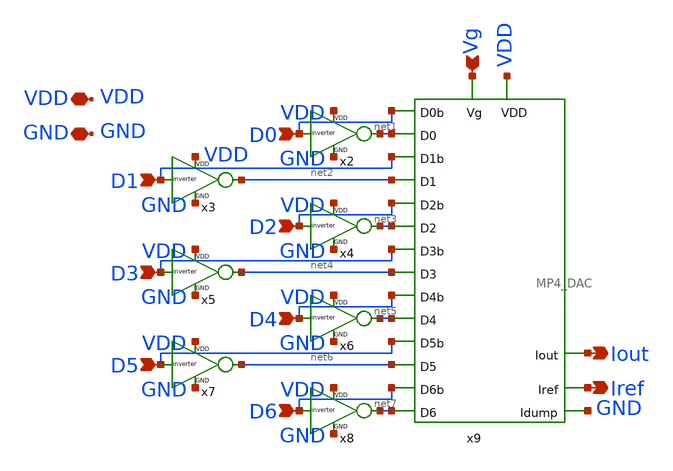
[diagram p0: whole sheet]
** sch_path: Final DAC files/schematics/DAC/simple_MP4_DAC.sch
**.subckt simple_MP4_DAC Iout D0 D1 D2 D3 D4 D5 D6 VDD GND Iref Vg
*.opin Iout
*.ipin D0
*.ipin D1
*.ipin D2
*.ipin D3
*.ipin D4
*.ipin D5
*.ipin D6
*.iopin VDD
*.iopin GND
*.opin Iref
*.ipin Vg
x2 VDD D0 net1 GND inverter
x3 VDD D1 net2 GND inverter
x4 VDD D2 net3 GND inverter
x5 VDD D3 net4 GND inverter
x6 VDD D4 net5 GND inverter
x7 VDD D5 net6 GND inverter
x8 VDD D6 net7 GND inverter
x9 VDD Vg net1 net3 net4 net5 net6 D5 net2 D0 D1 D2 D3 D4 net7 D6 Iref GND Iout MP4_DAC
**.ends

* expanding   symbol:  /home/madvlsi/dev/git/7-bit-D-A-converter-MP4-MADVLSI/schematics/ieee
*+ DAC/inverter.sym # of pins=4
** sym_path: schematics/ieee DAC/inverter.sym
** sch_path: schematics/ieee DAC/inverter.sch
.subckt inverter VDD A Y GND
*.ipin A
*.iopin VDD
*.iopin GND
*.opin Y
XM1 Y A GND GND sky130_fd_pr__nfet_01v8 L=0.5 W=12 nf=1 ad='int((nf+1)/2) * W/nf * 0.29' as='int((nf+2)/2) * W/nf * 0.29'
+ pd='2*int((nf+1)/2) * (W/nf + 0.29)' ps='2*int((nf+2)/2) * (W/nf + 0.29)' nrd='0.29 / W' nrs='0.29 / W'
+ sa=0 sb=0 sd=0 mult=1 m=1
XM2 Y A VDD VDD sky130_fd_pr__pfet_01v8 L=0.5 W=12 nf=1 ad='int((nf+1)/2) * W/nf * 0.29' as='int((nf+2)/2) * W/nf * 0.29'
+ pd='2*int((nf+1)/2) * (W/nf + 0.29)' ps='2*int((nf+2)/2) * (W/nf + 0.29)' nrd='0.29 / W' nrs='0.29 / W'
+ sa=0 sb=0 sd=0 mult=1 m=1
.ends


* expanding   symbol:  /home/madvlsi/dev/git/7-bit-D-A-converter-MP4-MADVLSI/Final DAC
*+ files/schematics/DAC/MP4_DAC.sym # of pins=19
** sym_path: Final DAC files/schematics/DAC/MP4_DAC.sym
** sch_path: Final DAC files/schematics/DAC/MP4_DAC.sch
.subckt MP4_DAC VDD Vg D0 D2 D3 D4 D5 D5b D1 D0b D1b D2b D3b D4b D6 D6b Iref Idump Iout
*.ipin Iout
*.ipin Vg
*.opin Iref
*.opin Idump
*.iopin VDD
*.ipin D0
*.ipin D1
*.ipin D2
*.ipin D3
*.ipin D4
*.ipin D5
*.ipin D6
*.ipin D0b
*.ipin D1b
*.ipin D2b
*.ipin D3b
*.ipin D4b
*.ipin D5b
*.ipin D6b
XM5 net7 Vg Iout GND sky130_fd_pr__nfet_01v8 L=4 W=16 nf=1 ad='int((nf+1)/2) * W/nf * 0.29' as='int((nf+2)/2) * W/nf * 0.29'
+ pd='2*int((nf+1)/2) * (W/nf + 0.29)' ps='2*int((nf+2)/2) * (W/nf + 0.29)' nrd='0.29 / W' nrs='0.29 / W'
+ sa=0 sb=0 sd=0 mult=2 m=2
XM8 net7 Vg net1 GND sky130_fd_pr__nfet_01v8 L=4 W=16 nf=1 ad='int((nf+1)/2) * W/nf * 0.29' as='int((nf+2)/2) * W/nf * 0.29'
+ pd='2*int((nf+1)/2) * (W/nf + 0.29)' ps='2*int((nf+2)/2) * (W/nf + 0.29)' nrd='0.29 / W' nrs='0.29 / W'
+ sa=0 sb=0 sd=0 mult=2 m=2
XM9 net1 Vg VDD GND sky130_fd_pr__nfet_01v8 L=4 W=16 nf=1 ad='int((nf+1)/2) * W/nf * 0.29' as='int((nf+2)/2) * W/nf * 0.29'
+ pd='2*int((nf+1)/2) * (W/nf + 0.29)' ps='2*int((nf+2)/2) * (W/nf + 0.29)' nrd='0.29 / W' nrs='0.29 / W'
+ sa=0 sb=0 sd=0 mult=1 m=1
XM12 net1 Vg net2 GND sky130_fd_pr__nfet_01v8 L=4 W=16 nf=1 ad='int((nf+1)/2) * W/nf * 0.29' as='int((nf+2)/2) * W/nf * 0.29'
+ pd='2*int((nf+1)/2) * (W/nf + 0.29)' ps='2*int((nf+2)/2) * (W/nf + 0.29)' nrd='0.29 / W' nrs='0.29 / W'
+ sa=0 sb=0 sd=0 mult=2 m=2
XM13 net2 Vg VDD GND sky130_fd_pr__nfet_01v8 L=4 W=16 nf=1 ad='int((nf+1)/2) * W/nf * 0.29' as='int((nf+2)/2) * W/nf * 0.29'
+ pd='2*int((nf+1)/2) * (W/nf + 0.29)' ps='2*int((nf+2)/2) * (W/nf + 0.29)' nrd='0.29 / W' nrs='0.29 / W'
+ sa=0 sb=0 sd=0 mult=1 m=1
XM16 net2 Vg net3 GND sky130_fd_pr__nfet_01v8 L=4 W=16 nf=1 ad='int((nf+1)/2) * W/nf * 0.29' as='int((nf+2)/2) * W/nf * 0.29'
+ pd='2*int((nf+1)/2) * (W/nf + 0.29)' ps='2*int((nf+2)/2) * (W/nf + 0.29)' nrd='0.29 / W' nrs='0.29 / W'
+ sa=0 sb=0 sd=0 mult=2 m=2
XM17 net3 Vg VDD GND sky130_fd_pr__nfet_01v8 L=4 W=16 nf=1 ad='int((nf+1)/2) * W/nf * 0.29' as='int((nf+2)/2) * W/nf * 0.29'
+ pd='2*int((nf+1)/2) * (W/nf + 0.29)' ps='2*int((nf+2)/2) * (W/nf + 0.29)' nrd='0.29 / W' nrs='0.29 / W'
+ sa=0 sb=0 sd=0 mult=1 m=1
XM7 net3 Vg net4 GND sky130_fd_pr__nfet_01v8 L=4 W=16 nf=1 ad='int((nf+1)/2) * W/nf * 0.29' as='int((nf+2)/2) * W/nf * 0.29'
+ pd='2*int((nf+1)/2) * (W/nf + 0.29)' ps='2*int((nf+2)/2) * (W/nf + 0.29)' nrd='0.29 / W' nrs='0.29 / W'
+ sa=0 sb=0 sd=0 mult=2 m=2
XM10 net4 Vg VDD GND sky130_fd_pr__nfet_01v8 L=4 W=16 nf=1 ad='int((nf+1)/2) * W/nf * 0.29' as='int((nf+2)/2) * W/nf * 0.29'
+ pd='2*int((nf+1)/2) * (W/nf + 0.29)' ps='2*int((nf+2)/2) * (W/nf + 0.29)' nrd='0.29 / W' nrs='0.29 / W'
+ sa=0 sb=0 sd=0 mult=1 m=1
XM15 net4 Vg net5 GND sky130_fd_pr__nfet_01v8 L=4 W=16 nf=1 ad='int((nf+1)/2) * W/nf * 0.29' as='int((nf+2)/2) * W/nf * 0.29'
+ pd='2*int((nf+1)/2) * (W/nf + 0.29)' ps='2*int((nf+2)/2) * (W/nf + 0.29)' nrd='0.29 / W' nrs='0.29 / W'
+ sa=0 sb=0 sd=0 mult=2 m=2
XM18 net5 Vg VDD GND sky130_fd_pr__nfet_01v8 L=4 W=16 nf=1 ad='int((nf+1)/2) * W/nf * 0.29' as='int((nf+2)/2) * W/nf * 0.29'
+ pd='2*int((nf+1)/2) * (W/nf + 0.29)' ps='2*int((nf+2)/2) * (W/nf + 0.29)' nrd='0.29 / W' nrs='0.29 / W'
+ sa=0 sb=0 sd=0 mult=1 m=1
XM28 net5 Vg net6 GND sky130_fd_pr__nfet_01v8 L=4 W=16 nf=1 ad='int((nf+1)/2) * W/nf * 0.29' as='int((nf+2)/2) * W/nf * 0.29'
+ pd='2*int((nf+1)/2) * (W/nf + 0.29)' ps='2*int((nf+2)/2) * (W/nf + 0.29)' nrd='0.29 / W' nrs='0.29 / W'
+ sa=0 sb=0 sd=0 mult=2 m=2
XM29 net6 Vg VDD GND sky130_fd_pr__nfet_01v8 L=4 W=16 nf=1 ad='int((nf+1)/2) * W/nf * 0.29' as='int((nf+2)/2) * W/nf * 0.29'
+ pd='2*int((nf+1)/2) * (W/nf + 0.29)' ps='2*int((nf+2)/2) * (W/nf + 0.29)' nrd='0.29 / W' nrs='0.29 / W'
+ sa=0 sb=0 sd=0 mult=2 m=2
XM1 net1 D5 Iref GND sky130_fd_pr__nfet_01v8 L=4 W=16 nf=1 ad='int((nf+1)/2) * W/nf * 0.29' as='int((nf+2)/2) * W/nf * 0.29'
+ pd='2*int((nf+1)/2) * (W/nf + 0.29)' ps='2*int((nf+2)/2) * (W/nf + 0.29)' nrd='0.29 / W' nrs='0.29 / W'
+ sa=0 sb=0 sd=0 mult=1 m=1
XM4 Idump D5b net1 GND sky130_fd_pr__nfet_01v8 L=4 W=16 nf=1 ad='int((nf+1)/2) * W/nf * 0.29' as='int((nf+2)/2) * W/nf * 0.29'
+ pd='2*int((nf+1)/2) * (W/nf + 0.29)' ps='2*int((nf+2)/2) * (W/nf + 0.29)' nrd='0.29 / W' nrs='0.29 / W'
+ sa=0 sb=0 sd=0 mult=1 m=1
XM30 net2 D4 Iref GND sky130_fd_pr__nfet_01v8 L=4 W=16 nf=1 ad='int((nf+1)/2) * W/nf * 0.29' as='int((nf+2)/2) * W/nf * 0.29'
+ pd='2*int((nf+1)/2) * (W/nf + 0.29)' ps='2*int((nf+2)/2) * (W/nf + 0.29)' nrd='0.29 / W' nrs='0.29 / W'
+ sa=0 sb=0 sd=0 mult=1 m=1
XM31 Idump D4b net2 GND sky130_fd_pr__nfet_01v8 L=4 W=16 nf=1 ad='int((nf+1)/2) * W/nf * 0.29' as='int((nf+2)/2) * W/nf * 0.29'
+ pd='2*int((nf+1)/2) * (W/nf + 0.29)' ps='2*int((nf+2)/2) * (W/nf + 0.29)' nrd='0.29 / W' nrs='0.29 / W'
+ sa=0 sb=0 sd=0 mult=1 m=1
XM32 net3 D3 Iref GND sky130_fd_pr__nfet_01v8 L=4 W=16 nf=1 ad='int((nf+1)/2) * W/nf * 0.29' as='int((nf+2)/2) * W/nf * 0.29'
+ pd='2*int((nf+1)/2) * (W/nf + 0.29)' ps='2*int((nf+2)/2) * (W/nf + 0.29)' nrd='0.29 / W' nrs='0.29 / W'
+ sa=0 sb=0 sd=0 mult=1 m=1
XM33 Idump D3b net3 GND sky130_fd_pr__nfet_01v8 L=4 W=16 nf=1 ad='int((nf+1)/2) * W/nf * 0.29' as='int((nf+2)/2) * W/nf * 0.29'
+ pd='2*int((nf+1)/2) * (W/nf + 0.29)' ps='2*int((nf+2)/2) * (W/nf + 0.29)' nrd='0.29 / W' nrs='0.29 / W'
+ sa=0 sb=0 sd=0 mult=1 m=1
XM34 net4 D2 Iref GND sky130_fd_pr__nfet_01v8 L=4 W=16 nf=1 ad='int((nf+1)/2) * W/nf * 0.29' as='int((nf+2)/2) * W/nf * 0.29'
+ pd='2*int((nf+1)/2) * (W/nf + 0.29)' ps='2*int((nf+2)/2) * (W/nf + 0.29)' nrd='0.29 / W' nrs='0.29 / W'
+ sa=0 sb=0 sd=0 mult=1 m=1
XM35 Idump D2b net4 GND sky130_fd_pr__nfet_01v8 L=4 W=16 nf=1 ad='int((nf+1)/2) * W/nf * 0.29' as='int((nf+2)/2) * W/nf * 0.29'
+ pd='2*int((nf+1)/2) * (W/nf + 0.29)' ps='2*int((nf+2)/2) * (W/nf + 0.29)' nrd='0.29 / W' nrs='0.29 / W'
+ sa=0 sb=0 sd=0 mult=1 m=1
XM36 net5 D1 Iref GND sky130_fd_pr__nfet_01v8 L=4 W=16 nf=1 ad='int((nf+1)/2) * W/nf * 0.29' as='int((nf+2)/2) * W/nf * 0.29'
+ pd='2*int((nf+1)/2) * (W/nf + 0.29)' ps='2*int((nf+2)/2) * (W/nf + 0.29)' nrd='0.29 / W' nrs='0.29 / W'
+ sa=0 sb=0 sd=0 mult=1 m=1
XM37 Idump D1b net5 GND sky130_fd_pr__nfet_01v8 L=4 W=16 nf=1 ad='int((nf+1)/2) * W/nf * 0.29' as='int((nf+2)/2) * W/nf * 0.29'
+ pd='2*int((nf+1)/2) * (W/nf + 0.29)' ps='2*int((nf+2)/2) * (W/nf + 0.29)' nrd='0.29 / W' nrs='0.29 / W'
+ sa=0 sb=0 sd=0 mult=1 m=1
XM38 net6 D0 Iref GND sky130_fd_pr__nfet_01v8 L=4 W=16 nf=1 ad='int((nf+1)/2) * W/nf * 0.29' as='int((nf+2)/2) * W/nf * 0.29'
+ pd='2*int((nf+1)/2) * (W/nf + 0.29)' ps='2*int((nf+2)/2) * (W/nf + 0.29)' nrd='0.29 / W' nrs='0.29 / W'
+ sa=0 sb=0 sd=0 mult=1 m=1
XM39 Idump D0b net6 GND sky130_fd_pr__nfet_01v8 L=4 W=16 nf=1 ad='int((nf+1)/2) * W/nf * 0.29' as='int((nf+2)/2) * W/nf * 0.29'
+ pd='2*int((nf+1)/2) * (W/nf + 0.29)' ps='2*int((nf+2)/2) * (W/nf + 0.29)' nrd='0.29 / W' nrs='0.29 / W'
+ sa=0 sb=0 sd=0 mult=1 m=1
XM40 net7 D6 Iref GND sky130_fd_pr__nfet_01v8 L=4 W=16 nf=1 ad='int((nf+1)/2) * W/nf * 0.29' as='int((nf+2)/2) * W/nf * 0.29'
+ pd='2*int((nf+1)/2) * (W/nf + 0.29)' ps='2*int((nf+2)/2) * (W/nf + 0.29)' nrd='0.29 / W' nrs='0.29 / W'
+ sa=0 sb=0 sd=0 mult=1 m=1
XM41 Idump D6b net7 GND sky130_fd_pr__nfet_01v8 L=4 W=16 nf=1 ad='int((nf+1)/2) * W/nf * 0.29' as='int((nf+2)/2) * W/nf * 0.29'
+ pd='2*int((nf+1)/2) * (W/nf + 0.29)' ps='2*int((nf+2)/2) * (W/nf + 0.29)' nrd='0.29 / W' nrs='0.29 / W'
+ sa=0 sb=0 sd=0 mult=1 m=1
.ends

.end
